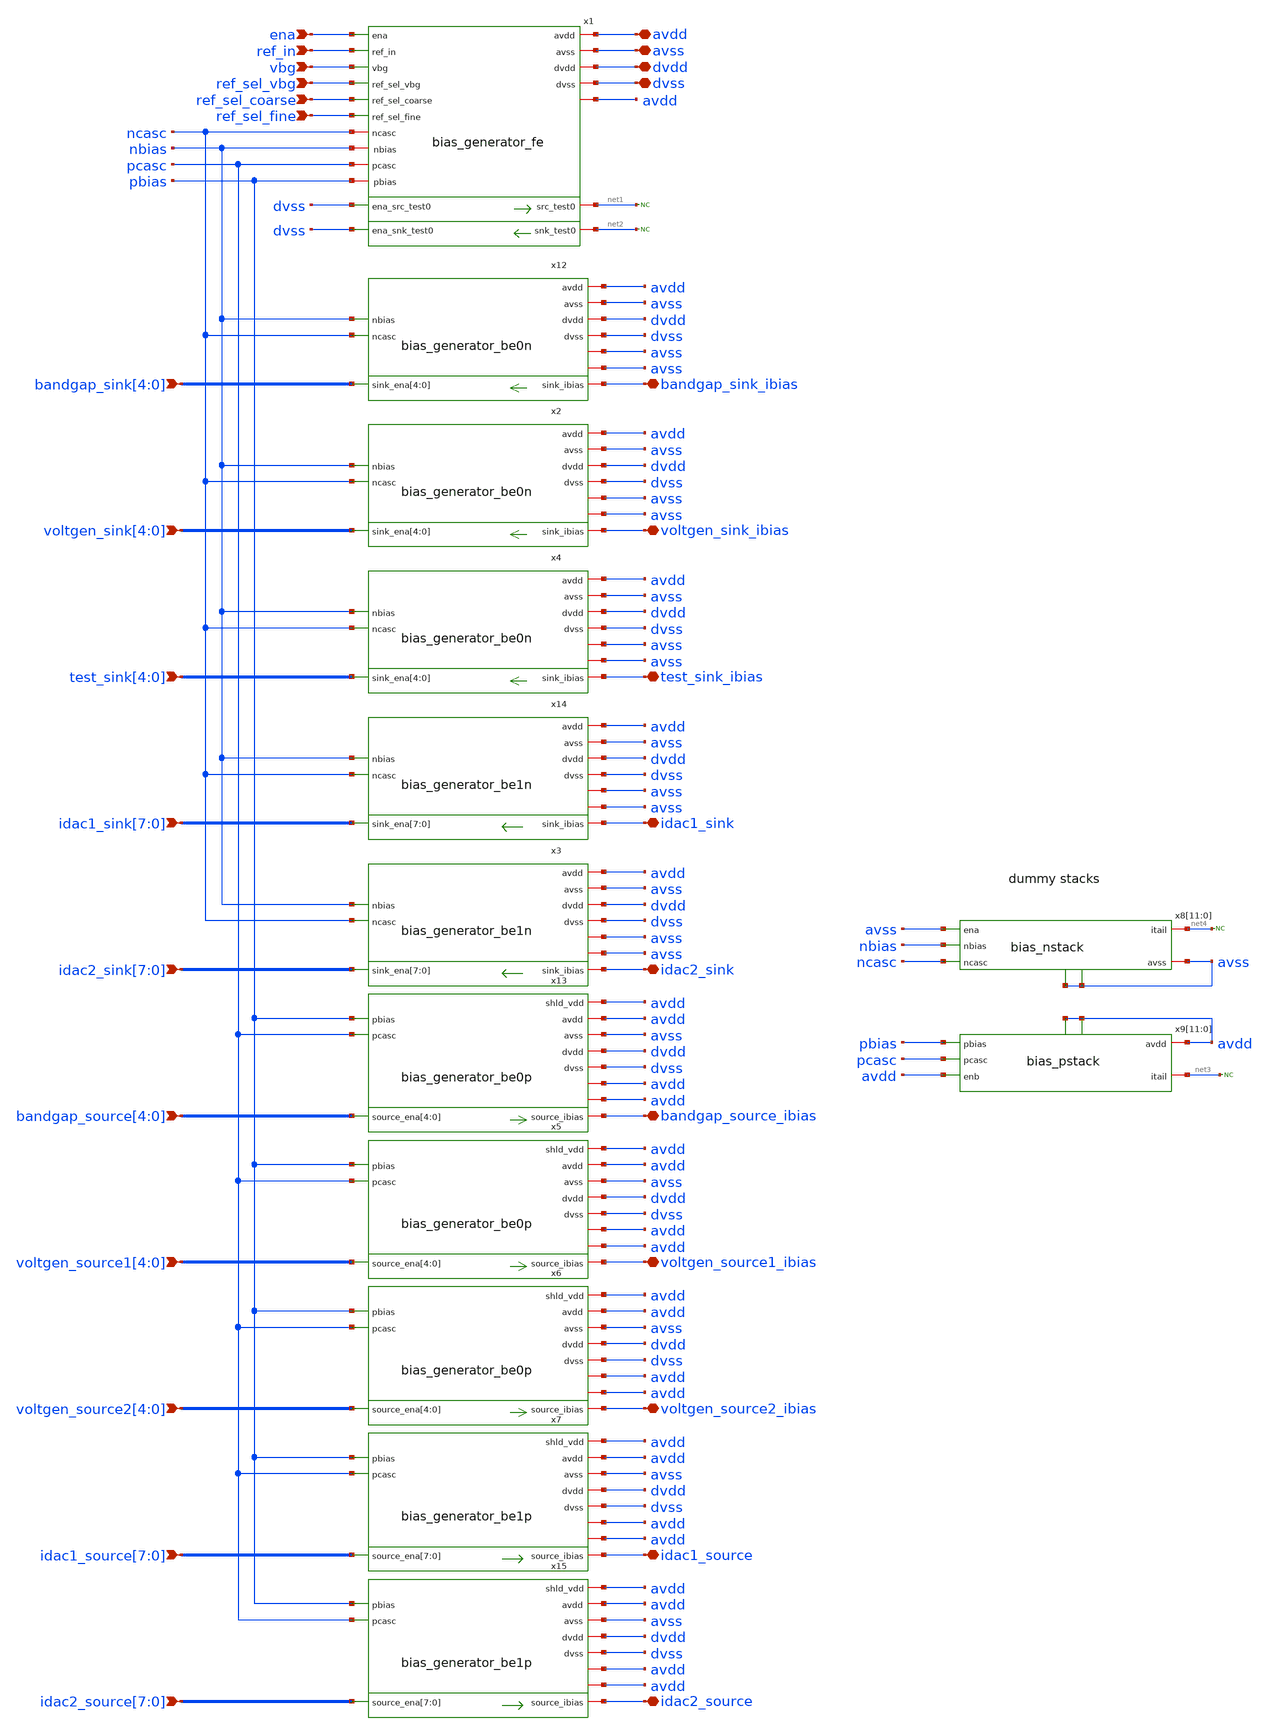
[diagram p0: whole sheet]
** sch_path: xschem/sg13cmos5l_ocd_ip__biasgen1.sch
**.subckt sg13cmos5l_ocd_ip__biasgen1 avdd avss dvdd dvss ena ref_in vbg ref_sel_vbg
*+ bandgap_sink[4],bandgap_sink[3],bandgap_sink[2],bandgap_sink[1],bandgap_sink[0] voltgen_sink[4],voltgen_sink[3],voltgen_sink[2],voltgen_sink[1],voltgen_sink[0]
*+ test_sink[4],test_sink[3],test_sink[2],test_sink[1],test_sink[0]
*+ idac1_sink[7],idac1_sink[6],idac1_sink[5],idac1_sink[4],idac1_sink[3],idac1_sink[2],idac1_sink[1],idac1_sink[0]
*+ idac2_sink[7],idac2_sink[6],idac2_sink[5],idac2_sink[4],idac2_sink[3],idac2_sink[2],idac2_sink[1],idac2_sink[0] bandgap_sink_ibias voltgen_sink_ibias test_sink_ibias idac1_sink idac2_sink ref_sel_fine
*+ ref_sel_coarse bandgap_source_ibias voltgen_source1_ibias voltgen_source2_ibias idac1_source idac2_source
*+ bandgap_source[4],bandgap_source[3],bandgap_source[2],bandgap_source[1],bandgap_source[0] voltgen_source1[4],voltgen_source1[3],voltgen_source1[2],voltgen_source1[1],voltgen_source1[0]
*+ voltgen_source2[4],voltgen_source2[3],voltgen_source2[2],voltgen_source2[1],voltgen_source2[0]
*+ idac1_source[7],idac1_source[6],idac1_source[5],idac1_source[4],idac1_source[3],idac1_source[2],idac1_source[1],idac1_source[0]
*+ idac2_source[7],idac2_source[6],idac2_source[5],idac2_source[4],idac2_source[3],idac2_source[2],idac2_source[1],idac2_source[0]
*.iopin avdd
*.iopin avss
*.iopin dvdd
*.iopin dvss
*.ipin ena
*.ipin ref_in
*.ipin vbg
*.ipin ref_sel_vbg
*.ipin bandgap_sink[4],bandgap_sink[3],bandgap_sink[2],bandgap_sink[1],bandgap_sink[0]
*.ipin voltgen_sink[4],voltgen_sink[3],voltgen_sink[2],voltgen_sink[1],voltgen_sink[0]
*.ipin test_sink[4],test_sink[3],test_sink[2],test_sink[1],test_sink[0]
*.ipin
*+ idac1_sink[7],idac1_sink[6],idac1_sink[5],idac1_sink[4],idac1_sink[3],idac1_sink[2],idac1_sink[1],idac1_sink[0]
*.ipin
*+ idac2_sink[7],idac2_sink[6],idac2_sink[5],idac2_sink[4],idac2_sink[3],idac2_sink[2],idac2_sink[1],idac2_sink[0]
*.iopin bandgap_sink_ibias
*.iopin voltgen_sink_ibias
*.iopin test_sink_ibias
*.iopin idac1_sink
*.iopin idac2_sink
*.ipin ref_sel_fine
*.ipin ref_sel_coarse
*.iopin bandgap_source_ibias
*.iopin voltgen_source1_ibias
*.iopin voltgen_source2_ibias
*.iopin idac1_source
*.iopin idac2_source
*.ipin bandgap_source[4],bandgap_source[3],bandgap_source[2],bandgap_source[1],bandgap_source[0]
*.ipin
*+ voltgen_source1[4],voltgen_source1[3],voltgen_source1[2],voltgen_source1[1],voltgen_source1[0]
*.ipin
*+ voltgen_source2[4],voltgen_source2[3],voltgen_source2[2],voltgen_source2[1],voltgen_source2[0]
*.ipin
*+ idac1_source[7],idac1_source[6],idac1_source[5],idac1_source[4],idac1_source[3],idac1_source[2],idac1_source[1],idac1_source[0]
*.ipin
*+ idac2_source[7],idac2_source[6],idac2_source[5],idac2_source[4],idac2_source[3],idac2_source[2],idac2_source[1],idac2_source[0]
x1 avdd ena vbg net1 avss dvdd dvss ref_sel_vbg ref_in dvss nbias pcasc pbias net2 dvss ncasc
+ ref_sel_fine ref_sel_coarse avdd bias_generator_fe
* noconn #net1
* noconn #net2
x12 dvdd dvss avdd nbias avss bandgap_sink[4] bandgap_sink[3] bandgap_sink[2] bandgap_sink[1]
+ bandgap_sink[0] bandgap_sink_ibias ncasc avss avss bias_generator_be0n
x13 dvdd dvss avdd pcasc pbias bandgap_source[4] bandgap_source[3] bandgap_source[2]
+ bandgap_source[1] bandgap_source[0] bandgap_source_ibias avss avdd avdd avdd bias_generator_be0p
x14 dvdd dvss avdd nbias avss idac1_sink[7] idac1_sink[6] idac1_sink[5] idac1_sink[4] idac1_sink[3]
+ idac1_sink[2] idac1_sink[1] idac1_sink[0] idac1_sink ncasc avss avss bias_generator_be1n
x15 dvdd dvss avdd pcasc pbias idac2_source[7] idac2_source[6] idac2_source[5] idac2_source[4]
+ idac2_source[3] idac2_source[2] idac2_source[1] idac2_source[0] idac2_source avss avdd avdd avdd
+ bias_generator_be1p
x2 dvdd dvss avdd nbias avss voltgen_sink[4] voltgen_sink[3] voltgen_sink[2] voltgen_sink[1]
+ voltgen_sink[0] voltgen_sink_ibias ncasc avss avss bias_generator_be0n
x4 dvdd dvss avdd nbias avss test_sink[4] test_sink[3] test_sink[2] test_sink[1] test_sink[0]
+ test_sink_ibias ncasc avss avss bias_generator_be0n
x3 dvdd dvss avdd nbias avss idac2_sink[7] idac2_sink[6] idac2_sink[5] idac2_sink[4] idac2_sink[3]
+ idac2_sink[2] idac2_sink[1] idac2_sink[0] idac2_sink ncasc avss avss bias_generator_be1n
x5 dvdd dvss avdd pcasc pbias voltgen_source1[4] voltgen_source1[3] voltgen_source1[2]
+ voltgen_source1[1] voltgen_source1[0] voltgen_source1_ibias avss avdd avdd avdd bias_generator_be0p
x6 dvdd dvss avdd pcasc pbias voltgen_source2[4] voltgen_source2[3] voltgen_source2[2]
+ voltgen_source2[1] voltgen_source2[0] voltgen_source2_ibias avss avdd avdd avdd bias_generator_be0p
x7 dvdd dvss avdd pcasc pbias idac1_source[7] idac1_source[6] idac1_source[5] idac1_source[4]
+ idac1_source[3] idac1_source[2] idac1_source[1] idac1_source[0] idac1_source avss avdd avdd avdd
+ bias_generator_be1p
x8[11] net4 avss ncasc nbias avss avss avss bias_nstack
x8[10] net4 avss ncasc nbias avss avss avss bias_nstack
x8[9] net4 avss ncasc nbias avss avss avss bias_nstack
x8[8] net4 avss ncasc nbias avss avss avss bias_nstack
x8[7] net4 avss ncasc nbias avss avss avss bias_nstack
x8[6] net4 avss ncasc nbias avss avss avss bias_nstack
x8[5] net4 avss ncasc nbias avss avss avss bias_nstack
x8[4] net4 avss ncasc nbias avss avss avss bias_nstack
x8[3] net4 avss ncasc nbias avss avss avss bias_nstack
x8[2] net4 avss ncasc nbias avss avss avss bias_nstack
x8[1] net4 avss ncasc nbias avss avss avss bias_nstack
x8[0] net4 avss ncasc nbias avss avss avss bias_nstack
x9[11] avdd pbias pcasc avdd net3 avdd avdd bias_pstack
x9[10] avdd pbias pcasc avdd net3 avdd avdd bias_pstack
x9[9] avdd pbias pcasc avdd net3 avdd avdd bias_pstack
x9[8] avdd pbias pcasc avdd net3 avdd avdd bias_pstack
x9[7] avdd pbias pcasc avdd net3 avdd avdd bias_pstack
x9[6] avdd pbias pcasc avdd net3 avdd avdd bias_pstack
x9[5] avdd pbias pcasc avdd net3 avdd avdd bias_pstack
x9[4] avdd pbias pcasc avdd net3 avdd avdd bias_pstack
x9[3] avdd pbias pcasc avdd net3 avdd avdd bias_pstack
x9[2] avdd pbias pcasc avdd net3 avdd avdd bias_pstack
x9[1] avdd pbias pcasc avdd net3 avdd avdd bias_pstack
x9[0] avdd pbias pcasc avdd net3 avdd avdd bias_pstack
* noconn #net4
* noconn #net3
**.ends
.end
